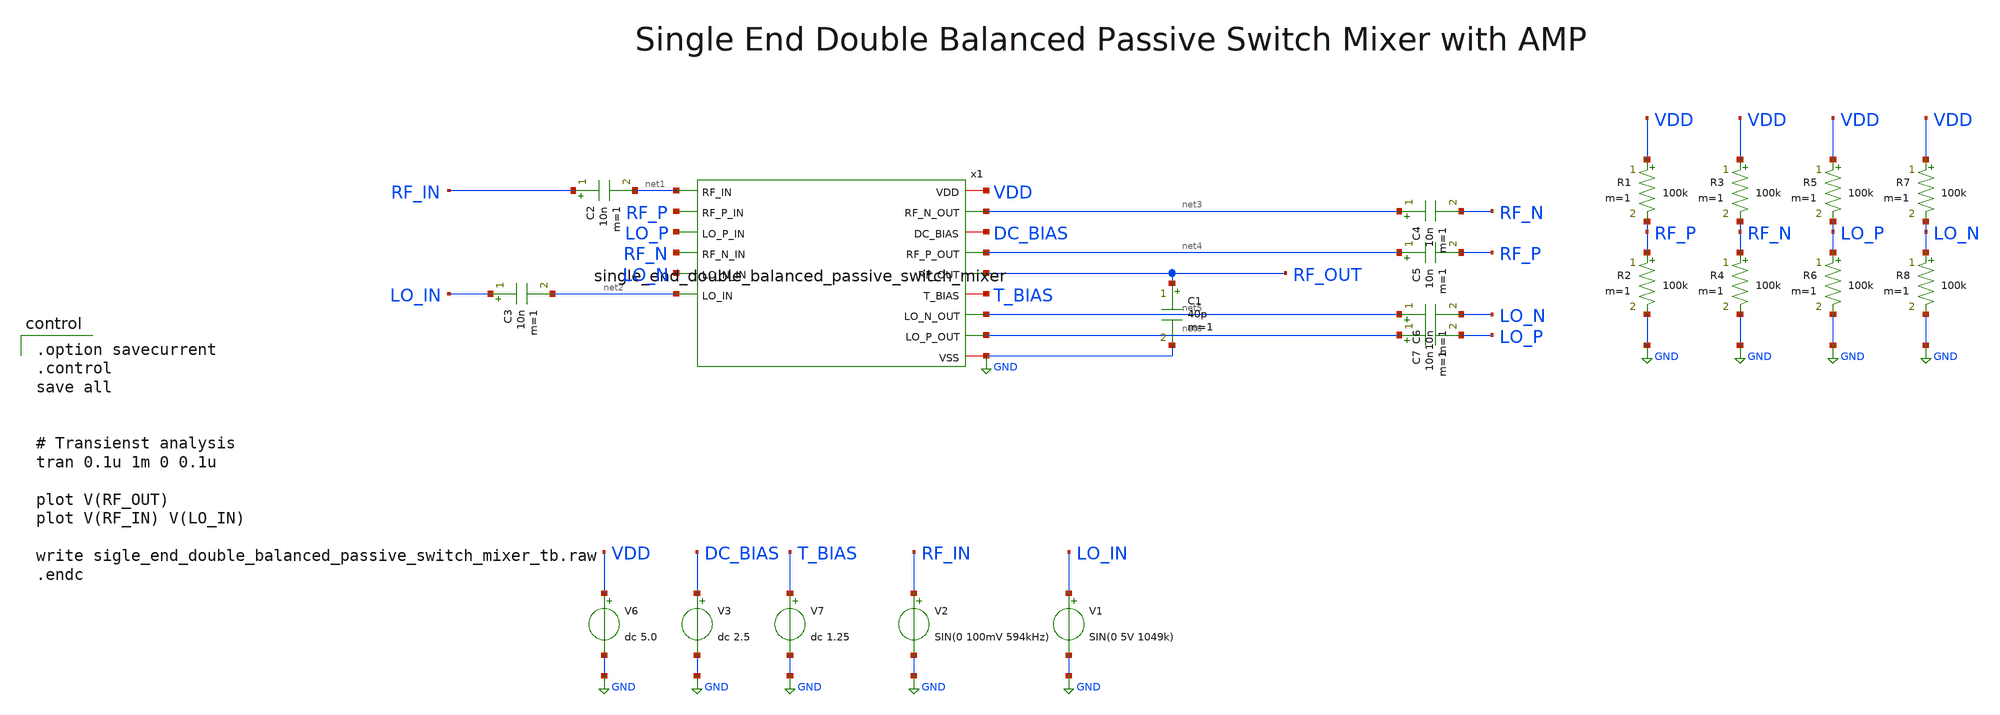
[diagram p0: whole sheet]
** sch_path: member_project/MIXER/noritsuna/xschem/single_end_double_balanced_passive_switch_mixer_tb.sch
**.subckt single_end_double_balanced_passive_switch_mixer_tb
V3 DC_BIAS GND dc 2.5
V6 VDD GND dc 5.0
V7 T_BIAS GND dc 1.25
V1 LO_IN GND SIN(0 5V 1049k)
V2 RF_IN GND SIN(0 100mV 594kHz)
C1 RF_OUT GND 40p m=1
x1 VDD net1 net3 RF_P DC_BIAS net4 LO_P RF_N RF_OUT LO_N T_BIAS net2 net5 net6 GND
+ single_end_double_balanced_passive_switch_mixer
C2 RF_IN net1 10n m=1
C3 LO_IN net2 10n m=1
C4 net3 RF_N 10n m=1
R1 VDD RF_P 100k m=1
R2 RF_P GND 100k m=1
R3 VDD RF_N 100k m=1
R4 RF_N GND 100k m=1
R5 VDD LO_P 100k m=1
R6 LO_P GND 100k m=1
R7 VDD LO_N 100k m=1
R8 LO_N GND 100k m=1
C5 net4 RF_P 10n m=1
C6 net5 LO_N 10n m=1
C7 net6 LO_P 10n m=1
**** begin user architecture code
 .include $::LIB/ip62_models

.option savecurrent
.control
save all


# Transienst analysis
tran 0.1u 1m 0 0.1u

plot V(RF_OUT)
plot V(RF_IN) V(LO_IN)

write sigle_end_double_balanced_passive_switch_mixer_tb.raw
.endc

**** end user architecture code
**.ends

* expanding   symbol:  single_end_double_balanced_passive_switch_mixer.sym # of pins=15
** sym_path: member_project/MIXER/noritsuna/xschem/single_end_double_balanced_passive_switch_mixer.sym
** sch_path: member_project/MIXER/noritsuna/xschem/single_end_double_balanced_passive_switch_mixer.sch
.subckt single_end_double_balanced_passive_switch_mixer VDD RF_IN RF_N_OUT RF_P_IN DC_BIAS RF_P_OUT
+ LO_P_IN RF_N_IN RF_OUT LO_N_IN T_BIAS LO_IN LO_N_OUT LO_P_OUT VSS
*.iopin DC_BIAS
*.iopin T_BIAS
*.ipin LO_IN
*.ipin RF_IN
*.iopin VDD
*.iopin VSS
*.opin RF_OUT
*.opin RF_N_OUT
*.opin RF_P_OUT
*.opin LO_P_OUT
*.opin LO_N_OUT
*.ipin RF_N_IN
*.ipin RF_P_IN
*.ipin LO_P_IN
*.ipin LO_N_IN
x2 DC_BIAS RF_P_IN VDD LO_P_IN RF_N_IN RF_OUT LO_N_IN VSS T_BIAS
+ double_balanced_passive_switch_mixer_w_amp
x1 VDD LO_N_OUT LO_IN LO_P_OUT VSS single_to_diff_LO
x3 VDD RF_N_OUT RF_IN RF_P_OUT VSS single_to_diff_RF
.ends


* expanding   symbol:  double_balanced_passive_switch_mixer_w_amp.sym # of pins=9
** sym_path: member_project/MIXER/noritsuna/xschem/double_balanced_passive_switch_mixer_w_amp.sym
** sch_path: member_project/MIXER/noritsuna/xschem/double_balanced_passive_switch_mixer_w_amp.sch
.subckt double_balanced_passive_switch_mixer_w_amp DC_BIAS RF_P VDD LO_P RF_N RF_OUT LO_N VSS T_BIAS
*.iopin T_BIAS
*.opin RF_OUT
*.ipin RF_P
*.ipin LO_P
*.ipin RF_N
*.ipin LO_N
*.iopin DC_BIAS
*.iopin VDD
*.iopin VSS
x1 VDD RF_OUT net1 net2 T_BIAS VSS diff_amp
x2 DC_BIAS RF_P LO_P RF_N LO_N net1 net2 VSS double_balanced_passive_switch_mixer
.ends


* expanding   symbol:  single_to_diff_LO.sym # of pins=5
** sym_path: member_project/MIXER/noritsuna/xschem/single_to_diff_LO.sym
** sch_path: member_project/MIXER/noritsuna/xschem/single_to_diff_LO.sch
.subckt single_to_diff_LO VDD LO_N LO_IN LO_P VSS
*.iopin VDD
*.iopin VSS
*.opin LO_N
*.opin LO_P
*.ipin LO_IN
XXM1 LO_N LO_IN LO_P VSS NMOS w=100u l=2u nrd=0 nrs=0 m=1
XR1 VDD LO_N VDD F_RR w=4.0e-06 l=15.8e-06 R=2.5e+03 tc1=0 tc2=0 m=1
XR2 LO_P VSS VDD F_RR w=4.0e-06 l=15.8e-06 R=2.5e+03 tc1=0 tc2=0 m=1
XR3 VDD LO_IN VDD F_RR w=2.8e-06 l=49.2e-06 R=20e+03 tc1=0 tc2=0 m=1
XR4 net1 VSS VDD F_RR w=2.8e-06 l=49.2e-06 R=40e+03 tc1=0 tc2=0 m=1
XXM6 LO_N VSS VSS VSS NMOS w=10u l=2u nrd=0 nrs=0 m=2
XR5 LO_IN net1 VDD F_RR w=2.8e-06 l=49.2e-06 R=40e+03 tc1=0 tc2=0 m=1
.ends


* expanding   symbol:  single_to_diff_RF.sym # of pins=5
** sym_path: member_project/MIXER/noritsuna/xschem/single_to_diff_RF.sym
** sch_path: member_project/MIXER/noritsuna/xschem/single_to_diff_RF.sch
.subckt single_to_diff_RF VDD RF_N RF_IN RF_P VSS
*.iopin VDD
*.iopin VSS
*.opin RF_N
*.opin RF_P
*.ipin RF_IN
XXM1 RF_N RF_IN RF_P VSS NMOS w=50u l=2u nrd=0 nrs=0 m=1
XR1 VDD RF_N VDD F_RR w=2.8e-06 l=17.8e-06 R=5e+03 tc1=0 tc2=0 m=1
XR2 RF_P VSS VDD F_RR w=2.8e-06 l=17.8e-06 R=5e+03 tc1=0 tc2=0 m=1
XR3 VDD RF_IN VDD F_RR w=2.8e-06 l=49.2e-06 R=20e+03 tc1=0 tc2=0 m=1
XR4 net1 VSS VDD F_RR w=2.8e-06 l=49.2e-06 R=40e+03 tc1=0 tc2=0 m=1
XXM6 RF_N VSS VSS VSS NMOS w=5u l=2u nrd=0 nrs=0 m=2
XR5 RF_IN net1 VDD F_RR w=2.8e-06 l=49.2e-06 R=40e+03 tc1=0 tc2=0 m=1
.ends


* expanding   symbol:  diff_amp.sym # of pins=6
** sym_path: member_project/MIXER/noritsuna/xschem/diff_amp.sym
** sch_path: member_project/MIXER/noritsuna/xschem/diff_amp.sch
.subckt diff_amp VDD RF_OUT IF_P IF_N T_BIAS VSS
*.ipin IF_P
*.ipin IF_N
*.ipin T_BIAS
*.iopin VDD
*.iopin VSS
*.opin RF_OUT
XXM1 DM_P_1 DM_P_1 VDD VDD PMOS w=50u l=2u nrd=0 nrs=0 m=1
XXM2 RF_OUT DM_P_1 VDD VDD PMOS w=50u l=2u nrd=0 nrs=0 m=1
XXM3 DM_P_1 IF_P DM_N_3 VSS NMOS w=50u l=1u nrd=0 nrs=0 m=1
XXM4 RF_OUT IF_N DM_N_3 VSS NMOS w=50u l=1u nrd=0 nrs=0 m=1
XXM5 DM_N_3 T_BIAS VSS VSS NMOS w=100u l=1u nrd=0 nrs=0 m=1
XXC2 RF_OUT VSS VSS F_CSIO c=960f x=40u y=40u m=4
XXM6 DM_P_1 VDD VDD VDD PMOS w=5u l=2u nrd=0 nrs=0 m=2
XXM7 RF_OUT VDD VDD VDD PMOS w=5u l=2u nrd=0 nrs=0 m=2
XXM8 DM_P_1 VSS VSS VSS NMOS w=5u l=1u nrd=0 nrs=0 m=2
XXM11 VSS VSS VSS VSS NMOS w=5u l=1u nrd=0 nrs=0 m=4
XXM9 RF_OUT VSS VSS VSS NMOS w=5u l=1u nrd=0 nrs=0 m=2
.ends


* expanding   symbol:  double_balanced_passive_switch_mixer.sym # of pins=8
** sym_path: member_project/MIXER/noritsuna/xschem/double_balanced_passive_switch_mixer.sym
** sch_path: member_project/MIXER/noritsuna/xschem/double_balanced_passive_switch_mixer.sch
.subckt double_balanced_passive_switch_mixer DC_BIAS RF_P LO_P RF_N LO_N IF_P IF_N VSS
*.iopin DC_BIAS
*.ipin RF_P
*.ipin LO_P
*.ipin RF_N
*.ipin LO_N
*.opin IF_N
*.opin IF_P
*.iopin VSS
XXM1 RF_P LO_P IF_P VSS NMOS w=100u l=1u nrd=0 nrs=0 m=1
XXM2 RF_P LO_N IF_N VSS NMOS w=100u l=1u nrd=0 nrs=0 m=1
XXM3 RF_N LO_N IF_P VSS NMOS w=100u l=1u nrd=0 nrs=0 m=1
XXM4 RF_N LO_P IF_N VSS NMOS w=100u l=1u nrd=0 nrs=0 m=1
XR1 DC_BIAS RF_P DC_BIAS F_RR w=2.8e-06 l=49.4e-06 R=20.0e+03 tc1=0 tc2=0 m=1
XR2 DC_BIAS IF_P DC_BIAS F_RR w=2.8e-06 l=49.4e-06 R=20.0e+03 tc1=0 tc2=0 m=1
XXC1 IF_P VSS VSS F_CSIO c=4.86p x=90u y=90u m=4
XXC2 IF_N VSS VSS F_CSIO c=4.86p x=90u y=90u m=4
XR3 DC_BIAS IF_N DC_BIAS F_RR w=2.8e-06 l=49.4e-06 R=20.0e+03 tc1=0 tc2=0 m=1
XXM6 IF_P VSS VSS VSS NMOS w=10u l=1u nrd=0 nrs=0 m=4
XXM7 IF_N VSS VSS VSS NMOS w=10u l=1u nrd=0 nrs=0 m=4
.ends

.GLOBAL GND
.end
